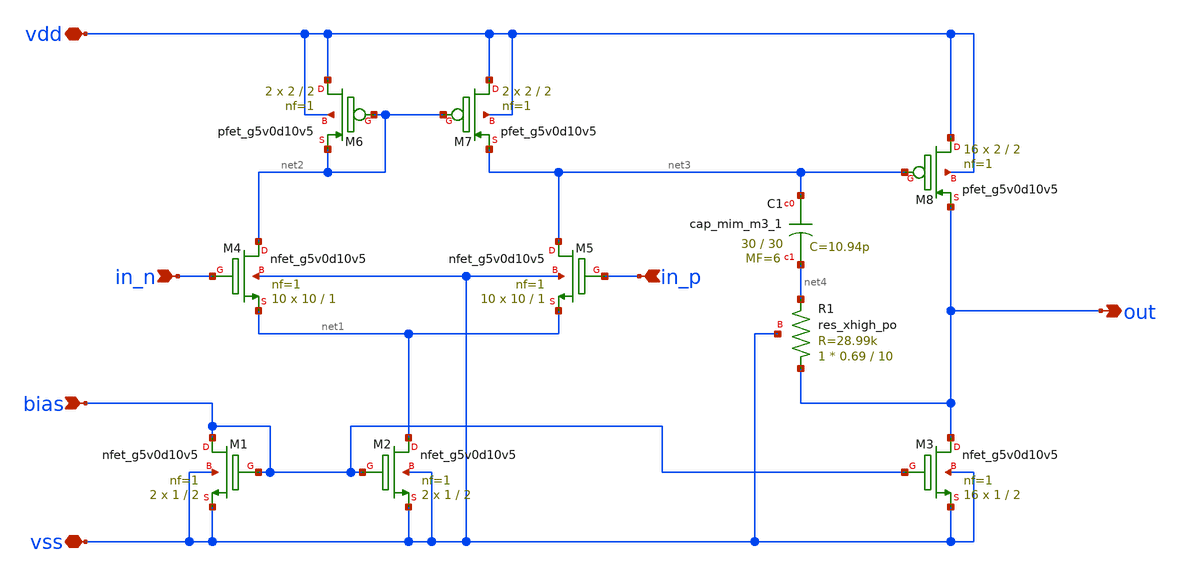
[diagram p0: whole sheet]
** sch_path: design/myopamp/myopamp.sch
**.subckt myopamp in_n in_p bias out vdd vss
*.ipin in_n
*.ipin in_p
*.ipin bias
*.opin out
*.iopin vdd
*.iopin vss
XM7 vdd net2 net3 vdd sky130_fd_pr__pfet_g5v0d10v5 L=2 W=2 nf=1 ad='int((nf+1)/2) * W/nf * 0.29' as='int((nf+2)/2) * W/nf * 0.29'
+ pd='2*int((nf+1)/2) * (W/nf + 0.29)' ps='2*int((nf+2)/2) * (W/nf + 0.29)' nrd='0.29 / W' nrs='0.29 / W'
+ sa=0 sb=0 sd=0 mult=2 m=2
XM6 vdd net2 net2 vdd sky130_fd_pr__pfet_g5v0d10v5 L=2 W=2 nf=1 ad='int((nf+1)/2) * W/nf * 0.29' as='int((nf+2)/2) * W/nf * 0.29'
+ pd='2*int((nf+1)/2) * (W/nf + 0.29)' ps='2*int((nf+2)/2) * (W/nf + 0.29)' nrd='0.29 / W' nrs='0.29 / W'
+ sa=0 sb=0 sd=0 mult=2 m=2
XM8 vdd net3 out vdd sky130_fd_pr__pfet_g5v0d10v5 L=2 W=2 nf=1 ad='int((nf+1)/2) * W/nf * 0.29' as='int((nf+2)/2) * W/nf * 0.29'
+ pd='2*int((nf+1)/2) * (W/nf + 0.29)' ps='2*int((nf+2)/2) * (W/nf + 0.29)' nrd='0.29 / W' nrs='0.29 / W'
+ sa=0 sb=0 sd=0 mult=16 m=16
XM4 net2 in_n net1 vss sky130_fd_pr__nfet_g5v0d10v5 L=1 W=10 nf=1 ad='int((nf+1)/2) * W/nf * 0.29' as='int((nf+2)/2) * W/nf * 0.29'
+ pd='2*int((nf+1)/2) * (W/nf + 0.29)' ps='2*int((nf+2)/2) * (W/nf + 0.29)' nrd='0.29 / W' nrs='0.29 / W'
+ sa=0 sb=0 sd=0 mult=10 m=10
XM5 net3 in_p net1 vss sky130_fd_pr__nfet_g5v0d10v5 L=1 W=10 nf=1 ad='int((nf+1)/2) * W/nf * 0.29' as='int((nf+2)/2) * W/nf * 0.29'
+ pd='2*int((nf+1)/2) * (W/nf + 0.29)' ps='2*int((nf+2)/2) * (W/nf + 0.29)' nrd='0.29 / W' nrs='0.29 / W'
+ sa=0 sb=0 sd=0 mult=10 m=10
XM1 bias bias vss vss sky130_fd_pr__nfet_g5v0d10v5 L=2 W=1 nf=1 ad='int((nf+1)/2) * W/nf * 0.29' as='int((nf+2)/2) * W/nf * 0.29'
+ pd='2*int((nf+1)/2) * (W/nf + 0.29)' ps='2*int((nf+2)/2) * (W/nf + 0.29)' nrd='0.29 / W' nrs='0.29 / W'
+ sa=0 sb=0 sd=0 mult=2 m=2
XM2 net1 bias vss vss sky130_fd_pr__nfet_g5v0d10v5 L=2 W=1 nf=1 ad='int((nf+1)/2) * W/nf * 0.29' as='int((nf+2)/2) * W/nf * 0.29'
+ pd='2*int((nf+1)/2) * (W/nf + 0.29)' ps='2*int((nf+2)/2) * (W/nf + 0.29)' nrd='0.29 / W' nrs='0.29 / W'
+ sa=0 sb=0 sd=0 mult=2 m=2
XM3 out bias vss vss sky130_fd_pr__nfet_g5v0d10v5 L=2 W=1 nf=1 ad='int((nf+1)/2) * W/nf * 0.29' as='int((nf+2)/2) * W/nf * 0.29'
+ pd='2*int((nf+1)/2) * (W/nf + 0.29)' ps='2*int((nf+2)/2) * (W/nf + 0.29)' nrd='0.29 / W' nrs='0.29 / W'
+ sa=0 sb=0 sd=0 mult=16 m=16
XC1 net3 net4 sky130_fd_pr__cap_mim_m3_1 W=30 L=30 MF=6 m=6
XR1 out net4 vss sky130_fd_pr__res_xhigh_po W=0.69 L=10 mult=1 m=1
**.ends
.end
